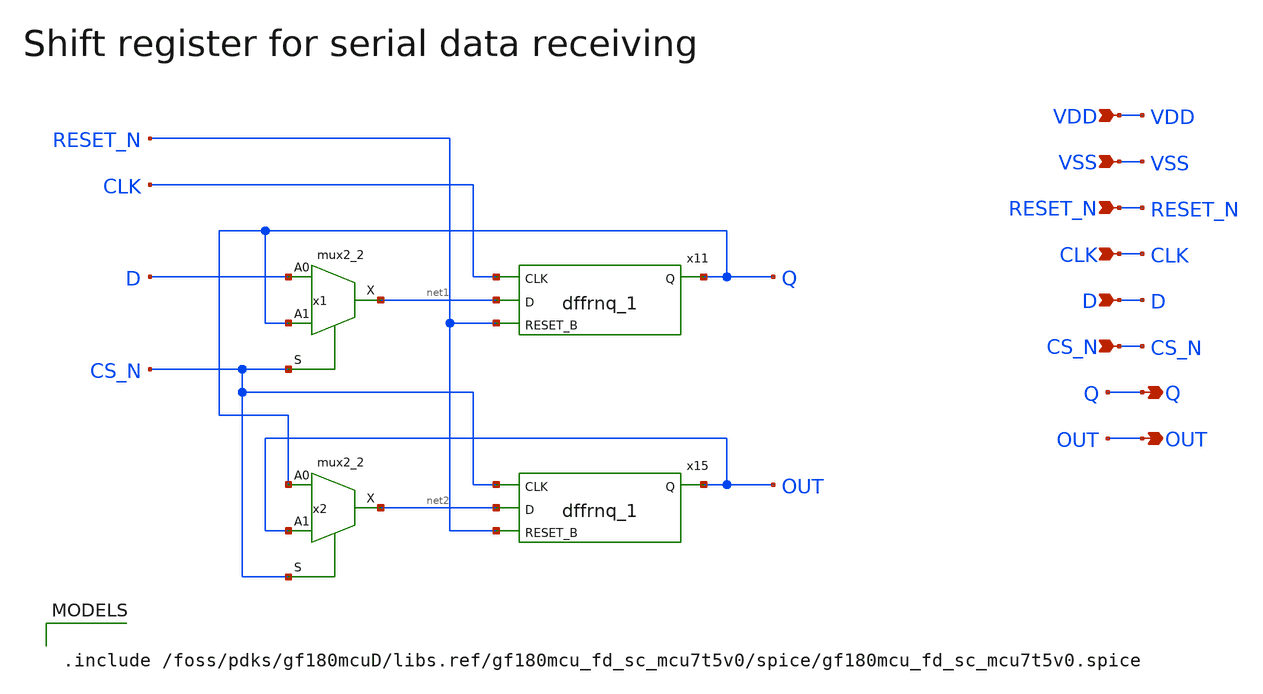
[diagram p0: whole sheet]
** sch_path: designs/libs/core_analog/sreg/sreg.sch
* Copyright 2022 GlobalFoundries PDK Authors
* Licensed under the Apache License, Version 2.0 (the "License");
* you may not use this file except in compliance with the License.
* You may obtain a copy of the License at
* https://www.apache.org/licenses/LICENSE-2.0
* Unless required by applicable law or agreed to in writing, software
* distributed under the License is distributed on an "AS IS" BASIS,
* WITHOUT WARRANTIES OR CONDITIONS OF ANY KIND, either express or implied.
* See the License for the specific language governing permissions and
* limitations under the License.
**.subckt sreg RESET_N CLK D CS_N VSS VDD Q OUT
*.ipin RESET_N
*.ipin CLK
*.ipin D
*.ipin CS_N
*.ipin VSS
*.ipin VDD
*.opin Q
*.opin OUT
x11 net1 RESET_N CLK Q VDD VDD VSS VSS gf180mcu_fd_sc_mcu7t5v0__dffrnq_1
x15 net2 RESET_N CS_N OUT VDD VDD VSS VSS gf180mcu_fd_sc_mcu7t5v0__dffrnq_1
x1 D Q CS_N net1 VDD VDD VSS VSS gf180mcu_fd_sc_mcu7t5v0__mux2_2
x2 Q OUT CS_N net2 VDD VDD VSS VSS gf180mcu_fd_sc_mcu7t5v0__mux2_2
**** begin user architecture code

.include /foss/pdks/gf180mcuD/libs.ref/gf180mcu_fd_sc_mcu7t5v0/spice/gf180mcu_fd_sc_mcu7t5v0.spice


**** end user architecture code
**.ends
.end
